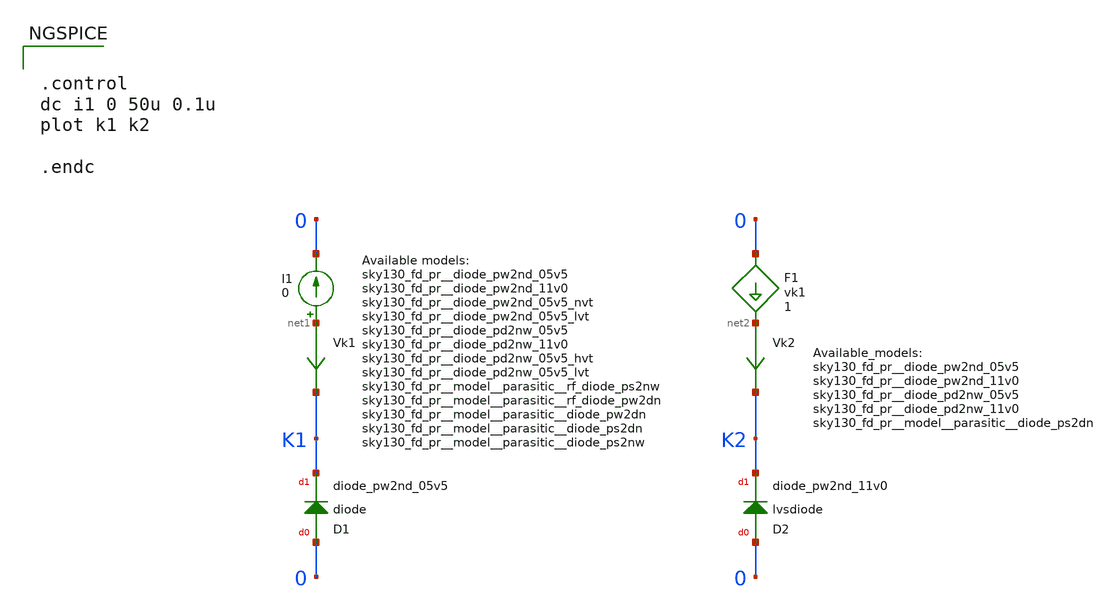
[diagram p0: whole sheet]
** sch_path: xyce/sky130A-xyce/libs.tech/xschem/sky130_tests/test_diode.sch
* Copyright 2020 Stefan Frederik Schippers
* Licensed under the Apache License, Version 2.0 (the "License");
* you may not use this file except in compliance with the License.
* You may obtain a copy of the License at
* https://www.apache.org/licenses/LICENSE-2.0
* Unless required by applicable law or agreed to in writing, software
* distributed under the License is distributed on an "AS IS" BASIS,
* WITHOUT WARRANTIES OR CONDITIONS OF ANY KIND, either express or implied.
* See the License for the specific language governing permissions and
* limitations under the License.
**.subckt test_diode
I1 net1 0 0
Vk1 net1 K1 0
.save i(vk1)
D1 0 K1 sky130_fd_pr__diode_pw2nd_05v5 area=1
Vk2 net2 K2 0
.save i(vk2)
D2 0 K2 sky130_fd_pr__diode_pw2nd_11v0 area=1
F1 0 net2 vk1 1
**** begin user architecture code


.control
dc i1 0 50u 0.1u
plot k1 k2

.endc



.include $::SKYWATER_MODELS/cells/nfet_01v8/sky130_fd_pr__nfet_01v8__tt.corner.spice
.include $::SKYWATER_MODELS/cells/nfet_01v8_lvt/sky130_fd_pr__nfet_01v8_lvt__tt.corner.spice
.include $::SKYWATER_MODELS/cells/pfet_01v8/sky130_fd_pr__pfet_01v8__tt.corner.spice
.include $::SKYWATER_MODELS/cells/nfet_03v3_nvt/sky130_fd_pr__nfet_03v3_nvt__tt.corner.spice
.include $::SKYWATER_MODELS/cells/nfet_05v0_nvt/sky130_fd_pr__nfet_05v0_nvt__tt.corner.spice
.include $::SKYWATER_MODELS/cells/esd_nfet_01v8/sky130_fd_pr__esd_nfet_01v8__tt.corner.spice
.include $::SKYWATER_MODELS/cells/pfet_01v8_lvt/sky130_fd_pr__pfet_01v8_lvt__tt.corner.spice
.include $::SKYWATER_MODELS/cells/pfet_01v8_hvt/sky130_fd_pr__pfet_01v8_hvt__tt.corner.spice
.include $::SKYWATER_MODELS/cells/esd_pfet_g5v0d10v5/sky130_fd_pr__esd_pfet_g5v0d10v5__tt.corner.spice
.include $::SKYWATER_MODELS/cells/pfet_g5v0d10v5/sky130_fd_pr__pfet_g5v0d10v5__tt.corner.spice
.include $::SKYWATER_MODELS/cells/pfet_g5v0d16v0/sky130_fd_pr__pfet_g5v0d16v0__tt.corner.spice
.include $::SKYWATER_MODELS/cells/nfet_g5v0d10v5/sky130_fd_pr__nfet_g5v0d10v5__tt.corner.spice
.include $::SKYWATER_MODELS/cells/nfet_g5v0d16v0/sky130_fd_pr__nfet_g5v0d16v0__tt_discrete.corner.spice
.include $::SKYWATER_MODELS/cells/esd_nfet_g5v0d10v5/sky130_fd_pr__esd_nfet_g5v0d10v5__tt.corner.spice
.include $::SKYWATER_MODELS/models/corners/tt/nonfet.spice
* Mismatch parameters
.include $::SKYWATER_MODELS/cells/nfet_01v8/sky130_fd_pr__nfet_01v8__mismatch.corner.spice
.include $::SKYWATER_MODELS/cells/pfet_01v8/sky130_fd_pr__pfet_01v8__mismatch.corner.spice
.include $::SKYWATER_MODELS/cells/nfet_01v8_lvt/sky130_fd_pr__nfet_01v8_lvt__mismatch.corner.spice
.include $::SKYWATER_MODELS/cells/pfet_01v8_lvt/sky130_fd_pr__pfet_01v8_lvt__mismatch.corner.spice
.include $::SKYWATER_MODELS/cells/pfet_01v8_hvt/sky130_fd_pr__pfet_01v8_hvt__mismatch.corner.spice
.include $::SKYWATER_MODELS/cells/nfet_g5v0d10v5/sky130_fd_pr__nfet_g5v0d10v5__mismatch.corner.spice
.include $::SKYWATER_MODELS/cells/pfet_g5v0d10v5/sky130_fd_pr__pfet_g5v0d10v5__mismatch.corner.spice
.include $::SKYWATER_MODELS/cells/nfet_05v0_nvt/sky130_fd_pr__nfet_05v0_nvt__mismatch.corner.spice
.include $::SKYWATER_MODELS/cells/nfet_03v3_nvt/sky130_fd_pr__nfet_03v3_nvt__mismatch.corner.spice
* Resistor$::SKYWATER_MODELS/Capacitor
.include $::SKYWATER_MODELS/models/r+c/res_typical__cap_typical.spice
.include $::SKYWATER_MODELS/models/r+c/res_typical__cap_typical__lin.spice
* Special cells
.include $::SKYWATER_MODELS/models/corners/tt/specialized_cells.spice
* All models
.include $::SKYWATER_MODELS/models/all.spice
* Corner
.include $::SKYWATER_MODELS/models/corners/tt/rf.spice

**** end user architecture code
**.ends
.end
